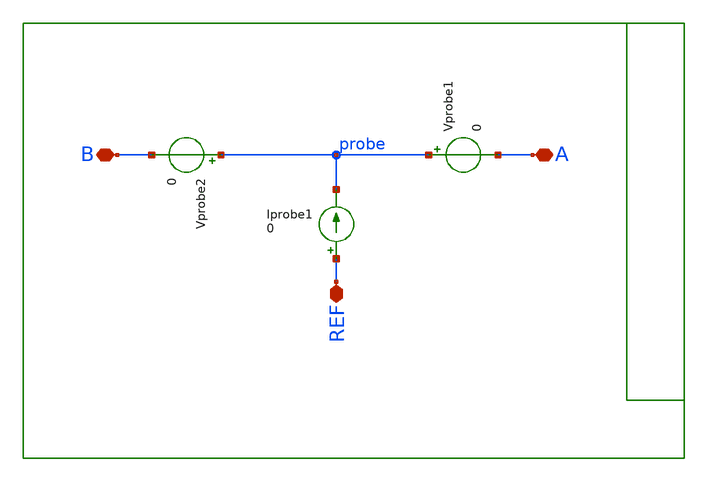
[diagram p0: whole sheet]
** sch_path: xschem/xschem/ideal/stbprobe/stbprobe.sch
**.subckt stbprobe A B REF
*.iopin A
*.iopin B
*.iopin REF
Vprobe1 probe A 0
Iprobe1 REF probe 0
Vprobe2 probe B 0
**** begin user architecture code



**** end user architecture code
**.ends
.end
